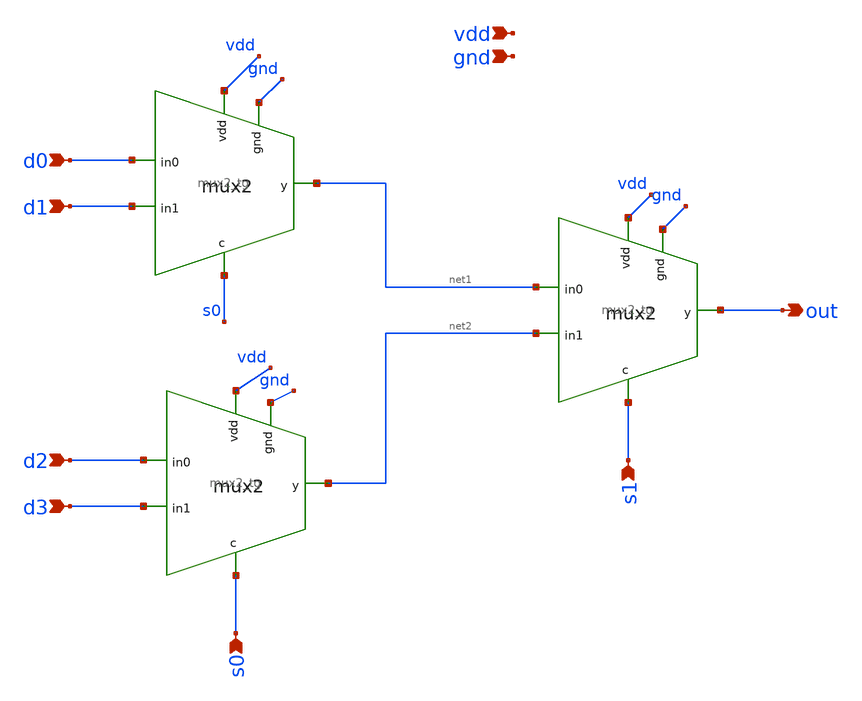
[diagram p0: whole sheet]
** sch_path: sram/mux4.sch
**.subckt mux4 d0 d1 d2 d3 s0 s1 out vdd gnd
*.ipin d0
*.ipin d1
*.ipin d2
*.ipin d3
*.ipin s0
*.ipin s1
*.opin out
*.ipin vdd
*.ipin gnd
x1 d0 s0 vdd gnd net1 d1 mux2_tg
x2 d2 s0 vdd gnd net2 d3 mux2_tg
x3 net1 s1 vdd gnd out net2 mux2_tg
**.ends

* expanding   symbol:  mux2_tg.sym # of pins=6
** sym_path: sram/mux2_tg.sym
** sch_path: sram/mux2_tg.sch
.subckt mux2_tg in0 c vdd gnd y in1
*.ipin in0
*.ipin in1
*.ipin c
*.opin y
*.ipin vdd
*.ipin gnd
XM5 y c in0 vdd sky130_fd_pr__pfet_01v8 L=0.15 W=1 nf=1 ad='int((nf+1)/2) * W/nf * 0.29' as='int((nf+2)/2) * W/nf * 0.29'
+ pd='2*int((nf+1)/2) * (W/nf + 0.29)' ps='2*int((nf+2)/2) * (W/nf + 0.29)' nrd='0.29 / W' nrs='0.29 / W'
+ sa=0 sb=0 sd=0 mult=1 m=1
XM2 in0 cb y gnd sky130_fd_pr__nfet_01v8 L=0.15 W=1 nf=1 ad='int((nf+1)/2) * W/nf * 0.29' as='int((nf+2)/2) * W/nf * 0.29'
+ pd='2*int((nf+1)/2) * (W/nf + 0.29)' ps='2*int((nf+2)/2) * (W/nf + 0.29)' nrd='0.29 / W' nrs='0.29 / W'
+ sa=0 sb=0 sd=0 mult=1 m=1
XM1 y cb in1 vdd sky130_fd_pr__pfet_01v8 L=0.15 W=1 nf=1 ad='int((nf+1)/2) * W/nf * 0.29' as='int((nf+2)/2) * W/nf * 0.29'
+ pd='2*int((nf+1)/2) * (W/nf + 0.29)' ps='2*int((nf+2)/2) * (W/nf + 0.29)' nrd='0.29 / W' nrs='0.29 / W'
+ sa=0 sb=0 sd=0 mult=1 m=1
XM3 in1 c y gnd sky130_fd_pr__nfet_01v8 L=0.15 W=1 nf=1 ad='int((nf+1)/2) * W/nf * 0.29' as='int((nf+2)/2) * W/nf * 0.29'
+ pd='2*int((nf+1)/2) * (W/nf + 0.29)' ps='2*int((nf+2)/2) * (W/nf + 0.29)' nrd='0.29 / W' nrs='0.29 / W'
+ sa=0 sb=0 sd=0 mult=1 m=1
x1 vdd c cb gnd inverter
.ends


* expanding   symbol:  inverter.sym # of pins=4
** sym_path: sram/inverter.sym
** sch_path: sram/inverter.sch
.subckt inverter vdd vin vout gnd
*.ipin vin
*.ipin vdd
*.ipin gnd
*.opin vout
XM1 vout vin gnd gnd sky130_fd_pr__nfet_01v8 L=0.15 W=1 nf=1 ad='int((nf+1)/2) * W/nf * 0.29' as='int((nf+2)/2) * W/nf * 0.29'
+ pd='2*int((nf+1)/2) * (W/nf + 0.29)' ps='2*int((nf+2)/2) * (W/nf + 0.29)' nrd='0.29 / W' nrs='0.29 / W'
+ sa=0 sb=0 sd=0 mult=1 m=1
XM2 vout vin vdd vdd sky130_fd_pr__pfet_01v8 L=0.15 W=1 nf=1 ad='int((nf+1)/2) * W/nf * 0.29' as='int((nf+2)/2) * W/nf * 0.29'
+ pd='2*int((nf+1)/2) * (W/nf + 0.29)' ps='2*int((nf+2)/2) * (W/nf + 0.29)' nrd='0.29 / W' nrs='0.29 / W'
+ sa=0 sb=0 sd=0 mult=1 m=1
.ends

.end
